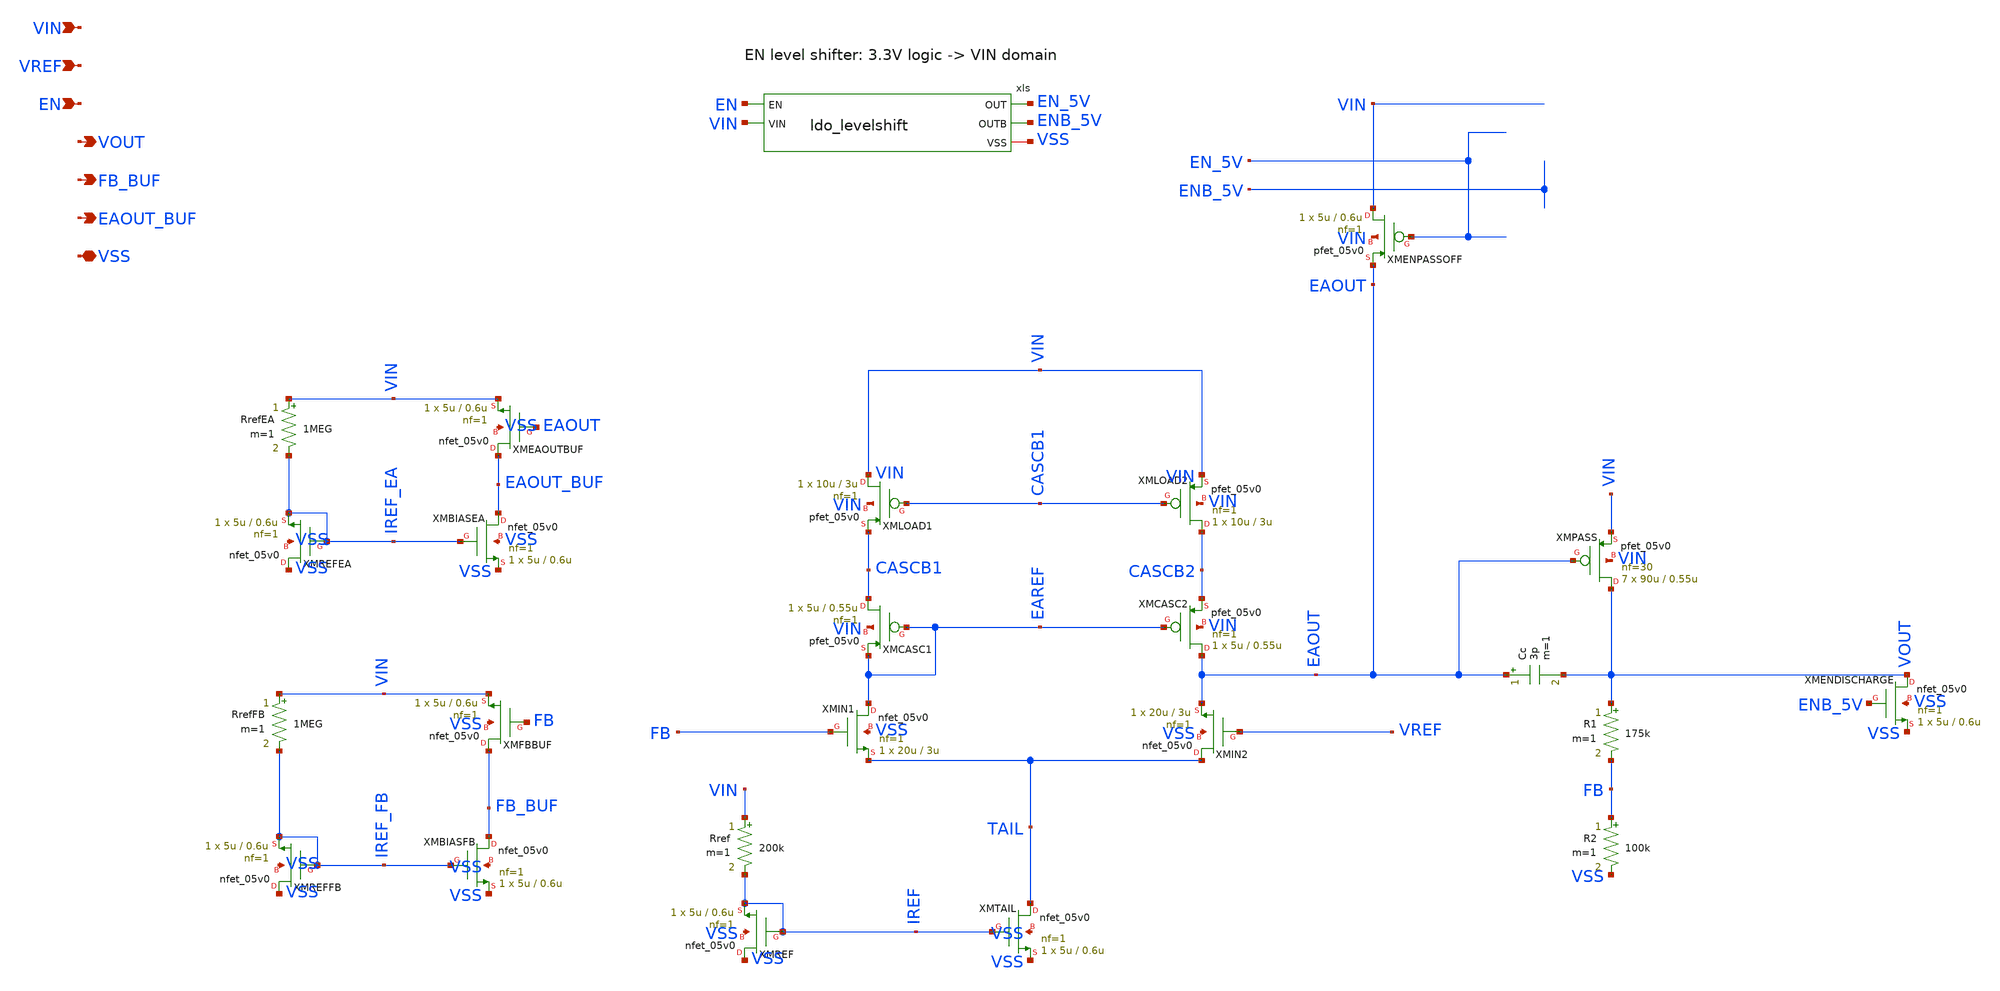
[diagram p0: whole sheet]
** sch_path: xschem/ldo.sch
**.subckt ldo VIN VREF EN VOUT FB_BUF EAOUT_BUF VSS
*.ipin VIN
*.ipin VREF
*.ipin EN
*.opin VOUT
*.opin FB_BUF
*.opin EAOUT_BUF
*.iopin VSS
Rref VIN IREF 200k m=1
XMREF VSS IREF IREF VSS nfet_05v0 L=0.6u W=5u nf=1 ad='int((nf+1)/2) * W/nf * 0.18u' as='int((nf+2)/2) * W/nf * 0.18u'
+ pd='2*int((nf+1)/2) * (W/nf + 0.18u)' ps='2*int((nf+2)/2) * (W/nf + 0.18u)' nrd='0.18u / W' nrs='0.18u / W'
+ sa=0 sb=0 sd=0 m=1
XMTAIL TAIL IREF VSS VSS nfet_05v0 L=0.6u W=5u nf=1 ad='int((nf+1)/2) * W/nf * 0.18u' as='int((nf+2)/2) * W/nf * 0.18u'
+ pd='2*int((nf+1)/2) * (W/nf + 0.18u)' ps='2*int((nf+2)/2) * (W/nf + 0.18u)' nrd='0.18u / W' nrs='0.18u / W'
+ sa=0 sb=0 sd=0 m=1
XMENPASSOFF VIN EN_5V EAOUT VIN pfet_05v0 L=0.6u W=5u nf=1 ad='int((nf+1)/2) * W/nf * 0.18u' as='int((nf+2)/2) * W/nf * 0.18u'
+ pd='2*int((nf+1)/2) * (W/nf + 0.18u)' ps='2*int((nf+2)/2) * (W/nf + 0.18u)' nrd='0.18u / W' nrs='0.18u / W'
+ sa=0 sb=0 sd=0 m=1
XMENDISCHARGE VOUT ENB_5V VSS VSS nfet_05v0 L=0.6u W=5u nf=1 ad='int((nf+1)/2) * W/nf * 0.18u' as='int((nf+2)/2) * W/nf * 0.18u'
+ pd='2*int((nf+1)/2) * (W/nf + 0.18u)' ps='2*int((nf+2)/2) * (W/nf + 0.18u)' nrd='0.18u / W' nrs='0.18u / W'
+ sa=0 sb=0 sd=0 m=1
RrefFB VIN IREF_FB 1MEG m=1
XMREFFB VSS IREF_FB IREF_FB VSS nfet_05v0 L=0.6u W=5u nf=1 ad='int((nf+1)/2) * W/nf * 0.18u' as='int((nf+2)/2) * W/nf * 0.18u'
+ pd='2*int((nf+1)/2) * (W/nf + 0.18u)' ps='2*int((nf+2)/2) * (W/nf + 0.18u)' nrd='0.18u / W' nrs='0.18u / W'
+ sa=0 sb=0 sd=0 m=1
XMFBBUF FB_BUF FB VIN VSS nfet_05v0 L=0.6u W=5u nf=1 ad='int((nf+1)/2) * W/nf * 0.18u' as='int((nf+2)/2) * W/nf * 0.18u'
+ pd='2*int((nf+1)/2) * (W/nf + 0.18u)' ps='2*int((nf+2)/2) * (W/nf + 0.18u)' nrd='0.18u / W' nrs='0.18u / W'
+ sa=0 sb=0 sd=0 m=1
XMBIASFB FB_BUF IREF_FB VSS VSS nfet_05v0 L=0.6u W=5u nf=1 ad='int((nf+1)/2) * W/nf * 0.18u' as='int((nf+2)/2) * W/nf * 0.18u'
+ pd='2*int((nf+1)/2) * (W/nf + 0.18u)' ps='2*int((nf+2)/2) * (W/nf + 0.18u)' nrd='0.18u / W' nrs='0.18u / W'
+ sa=0 sb=0 sd=0 m=1
RrefEA VIN IREF_EA 1MEG m=1
XMREFEA VSS IREF_EA IREF_EA VSS nfet_05v0 L=0.6u W=5u nf=1 ad='int((nf+1)/2) * W/nf * 0.18u' as='int((nf+2)/2) * W/nf * 0.18u'
+ pd='2*int((nf+1)/2) * (W/nf + 0.18u)' ps='2*int((nf+2)/2) * (W/nf + 0.18u)' nrd='0.18u / W' nrs='0.18u / W'
+ sa=0 sb=0 sd=0 m=1
XMEAOUTBUF EAOUT_BUF EAOUT VIN VSS nfet_05v0 L=0.6u W=5u nf=1 ad='int((nf+1)/2) * W/nf * 0.18u' as='int((nf+2)/2) * W/nf * 0.18u'
+ pd='2*int((nf+1)/2) * (W/nf + 0.18u)' ps='2*int((nf+2)/2) * (W/nf + 0.18u)' nrd='0.18u / W' nrs='0.18u / W'
+ sa=0 sb=0 sd=0 m=1
XMBIASEA EAOUT_BUF IREF_EA VSS VSS nfet_05v0 L=0.6u W=5u nf=1 ad='int((nf+1)/2) * W/nf * 0.18u' as='int((nf+2)/2) * W/nf * 0.18u'
+ pd='2*int((nf+1)/2) * (W/nf + 0.18u)' ps='2*int((nf+2)/2) * (W/nf + 0.18u)' nrd='0.18u / W' nrs='0.18u / W'
+ sa=0 sb=0 sd=0 m=1
XMIN1 EAREF FB TAIL VSS nfet_05v0 L=3u W=20u nf=1 ad='int((nf+1)/2) * W/nf * 0.18u' as='int((nf+2)/2) * W/nf * 0.18u'
+ pd='2*int((nf+1)/2) * (W/nf + 0.18u)' ps='2*int((nf+2)/2) * (W/nf + 0.18u)' nrd='0.18u / W' nrs='0.18u / W'
+ sa=0 sb=0 sd=0 m=1
XMIN2 TAIL VREF EAOUT VSS nfet_05v0 L=3u W=20u nf=1 ad='int((nf+1)/2) * W/nf * 0.18u' as='int((nf+2)/2) * W/nf * 0.18u'
+ pd='2*int((nf+1)/2) * (W/nf + 0.18u)' ps='2*int((nf+2)/2) * (W/nf + 0.18u)' nrd='0.18u / W' nrs='0.18u / W'
+ sa=0 sb=0 sd=0 m=1
XMLOAD1 VIN CASCB1 CASCB1 VIN pfet_05v0 L=3u W=10u nf=1 ad='int((nf+1)/2) * W/nf * 0.18u' as='int((nf+2)/2) * W/nf * 0.18u'
+ pd='2*int((nf+1)/2) * (W/nf + 0.18u)' ps='2*int((nf+2)/2) * (W/nf + 0.18u)' nrd='0.18u / W' nrs='0.18u / W'
+ sa=0 sb=0 sd=0 m=1
XMLOAD2 CASCB2 CASCB1 VIN VIN pfet_05v0 L=3u W=10u nf=1 ad='int((nf+1)/2) * W/nf * 0.18u' as='int((nf+2)/2) * W/nf * 0.18u'
+ pd='2*int((nf+1)/2) * (W/nf + 0.18u)' ps='2*int((nf+2)/2) * (W/nf + 0.18u)' nrd='0.18u / W' nrs='0.18u / W'
+ sa=0 sb=0 sd=0 m=1
XMPASS VOUT EAOUT VIN VIN pfet_05v0 L=0.55u W=90u nf=30 ad='int((nf+1)/2) * W/nf * 0.18u' as='int((nf+2)/2) * W/nf * 0.18u'
+ pd='2*int((nf+1)/2) * (W/nf + 0.18u)' ps='2*int((nf+2)/2) * (W/nf + 0.18u)' nrd='0.18u / W' nrs='0.18u / W'
+ sa=0 sb=0 sd=0 m=7
Cc EAOUT VOUT 3p m=1
R1 VOUT FB 175k m=1
R2 FB VSS 100k m=1
XMCASC1 CASCB1 EAREF EAREF VIN pfet_05v0 L=0.55u W=5u nf=1 ad='int((nf+1)/2) * W/nf * 0.18u' as='int((nf+2)/2) * W/nf * 0.18u'
+ pd='2*int((nf+1)/2) * (W/nf + 0.18u)' ps='2*int((nf+2)/2) * (W/nf + 0.18u)' nrd='0.18u / W' nrs='0.18u / W'
+ sa=0 sb=0 sd=0 m=1
XMCASC2 EAOUT EAREF CASCB2 VIN pfet_05v0 L=0.55u W=5u nf=1 ad='int((nf+1)/2) * W/nf * 0.18u' as='int((nf+2)/2) * W/nf * 0.18u'
+ pd='2*int((nf+1)/2) * (W/nf + 0.18u)' ps='2*int((nf+2)/2) * (W/nf + 0.18u)' nrd='0.18u / W' nrs='0.18u / W'
+ sa=0 sb=0 sd=0 m=1
xls EN VIN EN_5V ENB_5V VSS ldo_levelshift
**.ends

* expanding   symbol:  ldo_levelshift.sym # of pins=5
** sym_path: xschem/ldo_levelshift.sym
** sch_path: xschem/ldo_levelshift.sch
.subckt ldo_levelshift EN VIN OUT OUTB VSS
*.ipin EN
*.ipin VIN
*.opin OUT
*.opin OUTB
*.iopin VSS
XMP1 OUTB VSS VIN VIN pfet_05v0 L=40u W=1u nf=1 ad='int((nf+1)/2) * W/nf * 0.18u' as='int((nf+2)/2) * W/nf * 0.18u'
+ pd='2*int((nf+1)/2) * (W/nf + 0.18u)' ps='2*int((nf+2)/2) * (W/nf + 0.18u)' nrd='0.18u / W' nrs='0.18u / W'
+ sa=0 sb=0 sd=0 m=1
XMN1 OUTB EN VSS VSS nfet_05v0 L=5u W=0.5u nf=1 ad='int((nf+1)/2) * W/nf * 0.18u' as='int((nf+2)/2) * W/nf * 0.18u'
+ pd='2*int((nf+1)/2) * (W/nf + 0.18u)' ps='2*int((nf+2)/2) * (W/nf + 0.18u)' nrd='0.18u / W' nrs='0.18u / W'
+ sa=0 sb=0 sd=0 m=1
XMP2 OUT OUTB VIN VIN pfet_05v0 L=0.6u W=5u nf=1 ad='int((nf+1)/2) * W/nf * 0.18u' as='int((nf+2)/2) * W/nf * 0.18u'
+ pd='2*int((nf+1)/2) * (W/nf + 0.18u)' ps='2*int((nf+2)/2) * (W/nf + 0.18u)' nrd='0.18u / W' nrs='0.18u / W'
+ sa=0 sb=0 sd=0 m=1
XMN2 OUT OUTB VSS VSS nfet_05v0 L=0.6u W=5u nf=1 ad='int((nf+1)/2) * W/nf * 0.18u' as='int((nf+2)/2) * W/nf * 0.18u'
+ pd='2*int((nf+1)/2) * (W/nf + 0.18u)' ps='2*int((nf+2)/2) * (W/nf + 0.18u)' nrd='0.18u / W' nrs='0.18u / W'
+ sa=0 sb=0 sd=0 m=1
.ends

.end
